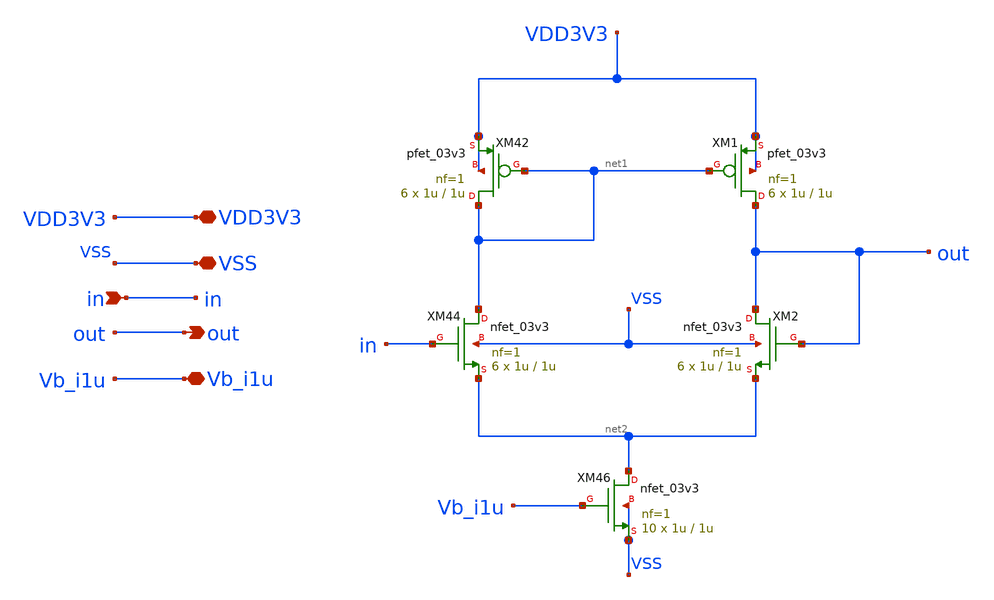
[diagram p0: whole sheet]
** sch_path: designs/libs/core_pga/buffer/core_buffer.sch
**.subckt core_buffer out VSS VDD3V3 in Vb_i1u
*.opin out
*.iopin VSS
*.iopin VDD3V3
*.ipin in
*.iopin Vb_i1u
XM42 net1 net1 VDD3V3 VDD3V3 pfet_03v3 L=1u W=1u nf=1 ad='int((nf+1)/2) * W/nf * 0.18u' as='int((nf+2)/2) * W/nf * 0.18u'
+ pd='2*int((nf+1)/2) * (W/nf + 0.18u)' ps='2*int((nf+2)/2) * (W/nf + 0.18u)' nrd='0.18u / W' nrs='0.18u / W'
+ sa=0 sb=0 sd=0 m=6
XM44 net1 in net2 VSS nfet_03v3 L=1u W=1u nf=1 ad='int((nf+1)/2) * W/nf * 0.18u' as='int((nf+2)/2) * W/nf * 0.18u'
+ pd='2*int((nf+1)/2) * (W/nf + 0.18u)' ps='2*int((nf+2)/2) * (W/nf + 0.18u)' nrd='0.18u / W' nrs='0.18u / W'
+ sa=0 sb=0 sd=0 m=6
XM46 net2 Vb_i1u VSS VSS nfet_03v3 L=1u W=1u nf=1 ad='int((nf+1)/2) * W/nf * 0.18u' as='int((nf+2)/2) * W/nf * 0.18u'
+ pd='2*int((nf+1)/2) * (W/nf + 0.18u)' ps='2*int((nf+2)/2) * (W/nf + 0.18u)' nrd='0.18u / W' nrs='0.18u / W'
+ sa=0 sb=0 sd=0 m=10
XM1 out net1 VDD3V3 VDD3V3 pfet_03v3 L=1u W=1u nf=1 ad='int((nf+1)/2) * W/nf * 0.18u' as='int((nf+2)/2) * W/nf * 0.18u'
+ pd='2*int((nf+1)/2) * (W/nf + 0.18u)' ps='2*int((nf+2)/2) * (W/nf + 0.18u)' nrd='0.18u / W' nrs='0.18u / W'
+ sa=0 sb=0 sd=0 m=6
XM2 out out net2 VSS nfet_03v3 L=1u W=1u nf=1 ad='int((nf+1)/2) * W/nf * 0.18u' as='int((nf+2)/2) * W/nf * 0.18u'
+ pd='2*int((nf+1)/2) * (W/nf + 0.18u)' ps='2*int((nf+2)/2) * (W/nf + 0.18u)' nrd='0.18u / W' nrs='0.18u / W'
+ sa=0 sb=0 sd=0 m=6
**.ends
.end
